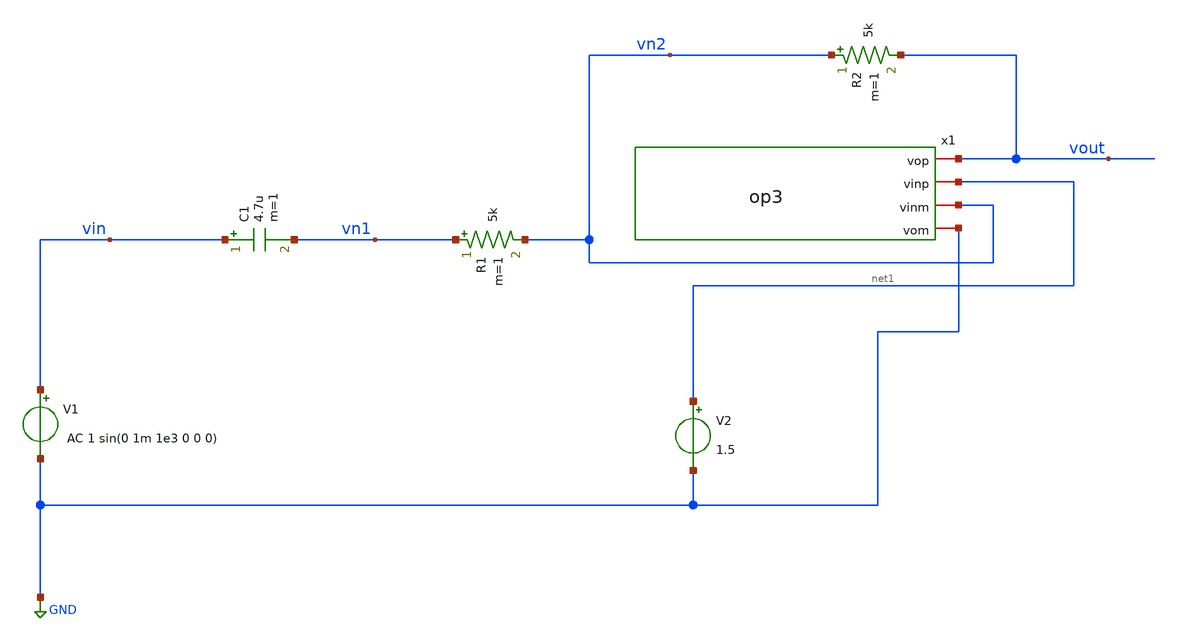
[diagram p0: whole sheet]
** sch_path: xschem/untitled-2.sch
**.subckt untitled-2
x1 vout net1 vn2 GND op3
R1 vn1 vn2 5k m=1
R2 vn2 vout 5k m=1
C1 vin vn1 4.7u m=1
V1 vin GND AC 1 sin(0 1m 1e3 0 0 0)
V2 net1 GND 1.5
**.ends

* expanding   symbol:  op3.sym # of pins=4
** sym_path: xschem/op3.sym
** sch_path: xschem/op3.sch
.subckt op3 vop vinp vinm vom
*.iopin vinp
*.iopin vinm
*.iopin vop
*.iopin vom
E1 net1 net3 vinp vinm 1000
E2 vop vom net2 net3 1000
R1 net1 net2 1k m=1
C1 net2 net3 160n m=1
.ends

.GLOBAL GND
.end
